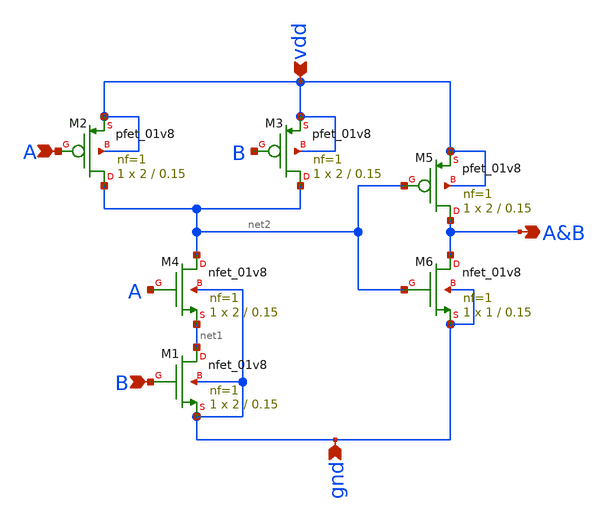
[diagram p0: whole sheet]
** sch_path: schematics/and.sch
**.subckt and gnd vdd A B A&B
*.ipin gnd
*.ipin vdd
*.ipin A
*.ipin B
*.opin A&B
XM6 A&B net2 gnd gnd sky130_fd_pr__nfet_01v8 L=0.15 W=1 nf=1 ad='int((1 + 1)/2) * 1 / 1 * 0.29' as='int((1 + 2)/2) * 1 / 1 * 0.29'
+ pd='2*int((1 + 1)/2) * (1 / 1 + 0.29)' ps='2*int((1 + 2)/2) * (1 / 1 + 0.29)' nrd='0.29 / 1 ' nrs='0.29 / 1 '
+ sa=0 sb=0 sd=0 mult=1 m=1
XM1 net1 B gnd gnd sky130_fd_pr__nfet_01v8 L=0.15 W=2 nf=1 ad='int((1 + 1)/2) * 2 / 1 * 0.29' as='int((1 + 2)/2) * 2 / 1 * 0.29'
+ pd='2*int((1 + 1)/2) * (2 / 1 + 0.29)' ps='2*int((1 + 2)/2) * (2 / 1 + 0.29)' nrd='0.29 / 2 ' nrs='0.29 / 2 '
+ sa=0 sb=0 sd=0 mult=1 m=1
XM2 net2 A vdd vdd sky130_fd_pr__pfet_01v8 L=0.15 W=2 nf=1 ad='int((1 + 1)/2) * 2 / 1 * 0.29' as='int((1 + 2)/2) * 2 / 1 * 0.29'
+ pd='2*int((1 + 1)/2) * (2 / 1 + 0.29)' ps='2*int((1 + 2)/2) * (2 / 1 + 0.29)' nrd='0.29 / 2 ' nrs='0.29 / 2 '
+ sa=0 sb=0 sd=0 mult=1 m=1
XM3 net2 B vdd vdd sky130_fd_pr__pfet_01v8 L=0.15 W=2 nf=1 ad='int((1 + 1)/2) * 2 / 1 * 0.29' as='int((1 + 2)/2) * 2 / 1 * 0.29'
+ pd='2*int((1 + 1)/2) * (2 / 1 + 0.29)' ps='2*int((1 + 2)/2) * (2 / 1 + 0.29)' nrd='0.29 / 2 ' nrs='0.29 / 2 '
+ sa=0 sb=0 sd=0 mult=1 m=1
XM4 net2 A net1 gnd sky130_fd_pr__nfet_01v8 L=0.15 W=2 nf=1 ad='int((1 + 1)/2) * 2 / 1 * 0.29' as='int((1 + 2)/2) * 2 / 1 * 0.29'
+ pd='2*int((1 + 1)/2) * (2 / 1 + 0.29)' ps='2*int((1 + 2)/2) * (2 / 1 + 0.29)' nrd='0.29 / 2 ' nrs='0.29 / 2 '
+ sa=0 sb=0 sd=0 mult=1 m=1
XM5 A&B net2 vdd vdd sky130_fd_pr__pfet_01v8 L=0.15 W=2 nf=1 ad='int((1 + 1)/2) * 2 / 1 * 0.29' as='int((1 + 2)/2) * 2 / 1 * 0.29'
+ pd='2*int((1 + 1)/2) * (2 / 1 + 0.29)' ps='2*int((1 + 2)/2) * (2 / 1 + 0.29)' nrd='0.29 / 2 ' nrs='0.29 / 2 '
+ sa=0 sb=0 sd=0 mult=1 m=1
**.ends
.end
